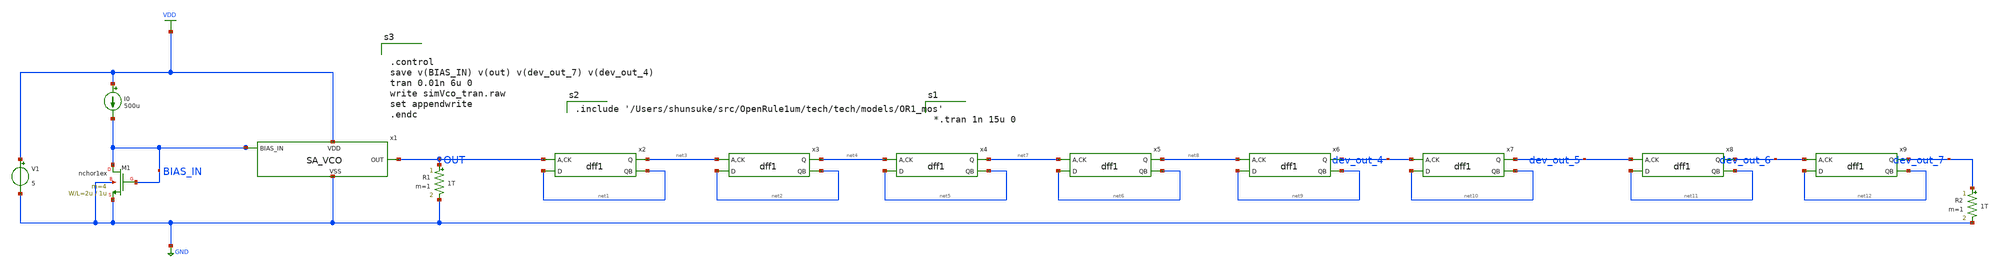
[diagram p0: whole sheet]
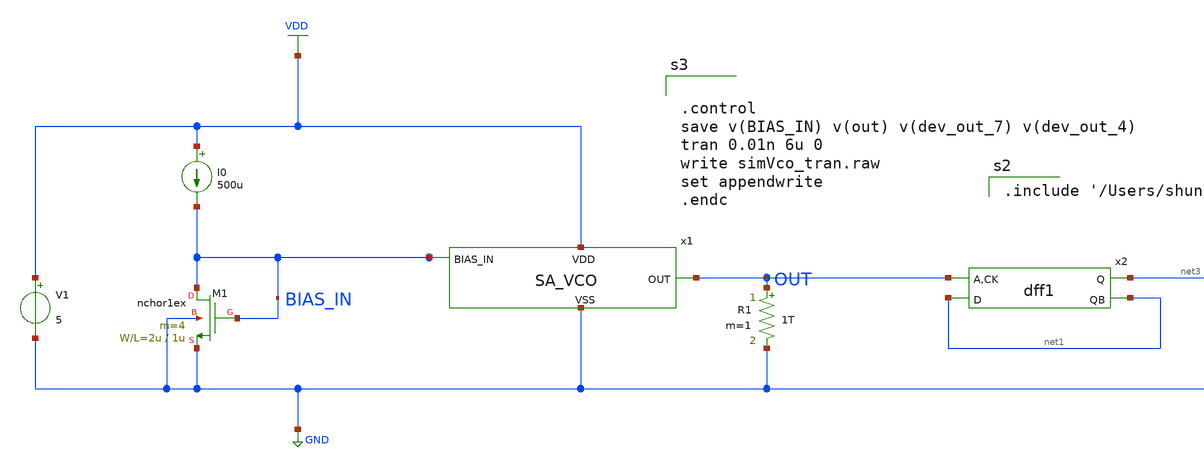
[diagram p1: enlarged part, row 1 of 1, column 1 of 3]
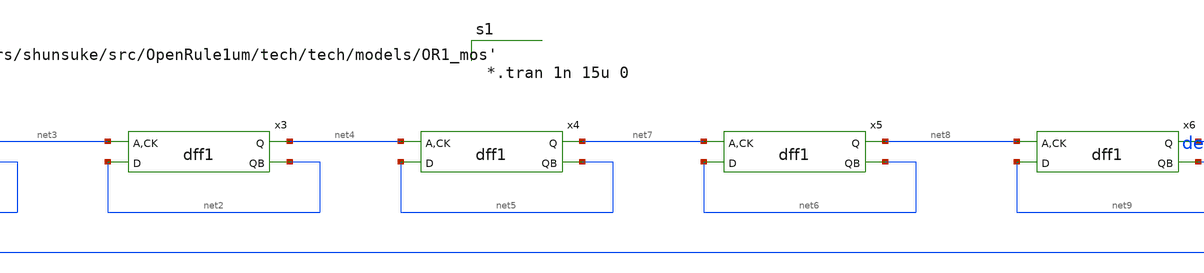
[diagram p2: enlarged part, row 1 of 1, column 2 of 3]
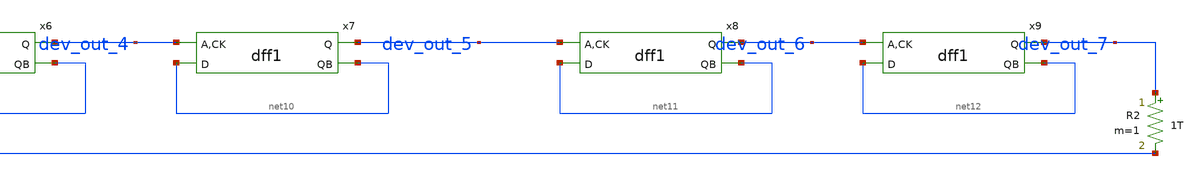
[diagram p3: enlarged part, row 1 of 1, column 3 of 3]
** sch_path: design/.design_bk/xschem/testbench/testVco.sch
**.subckt testVco
V1 VDD GND 5
.save i(v1)
x1 VDD OUT BIAS_IN GND SA_VCO
R1 OUT GND 1T m=1
M1 BIAS_IN BIAS_IN GND GND nchor1ex L=1u W=2u m=4
I0 VDD BIAS_IN 500u
x2 OUT OUT net1 VDD GND net3 net1 dff1
x3 net3 net3 net2 VDD GND net4 net2 dff1
x4 net4 net4 net5 VDD GND net7 net5 dff1
x5 net7 net7 net6 VDD GND net8 net6 dff1
x6 net8 net8 net9 VDD GND dev_out_4 net9 dff1
x7 dev_out_4 dev_out_4 net10 VDD GND dev_out_5 net10 dff1
R2 dev_out_7 GND 1T m=1
x8 dev_out_5 dev_out_5 net11 VDD GND dev_out_6 net11 dff1
x9 dev_out_6 dev_out_6 net12 VDD GND dev_out_7 net12 dff1
**** begin user architecture code


*.tran 1n 15u 0



.include '/Users/shunsuke/src/OpenRule1um/tech/tech/models/OR1_mos'



.control
save v(BIAS_IN) v(out) v(dev_out_7) v(dev_out_4)
tran 0.01n 6u 0
write simVco_tran.raw
set appendwrite
.endc


**** end user architecture code
**.ends

* expanding   symbol:  VCO/SA_VCO.sym # of pins=4
** sym_path: design/xschem/VCO/SA_VCO.sym
** sch_path: design/xschem/VCO/SA_VCO.sch
.subckt SA_VCO VDD OUT BIAS_IN VSS
*.iopin VDD
*.iopin VSS
*.ipin BIAS_IN
*.opin OUT
x1 VDD VDD VSS net1 OUT RO_9
M1 net1 BIAS_IN VSS VSS nchor1ex L=1u W=2u m=4
M2 VSS VSS VSS VSS nchor1ex L=1u W=2u m=2
.ends


* expanding   symbol:  VCO/RO_9.sym # of pins=5
** sym_path: design/.design_bk/xschem/VCO/RO_9.sym
** sch_path: design/.design_bk/xschem/VCO/RO_9.sch
.subckt RO_9 pchSource VDD VSS nchSource OUT
*.iopin pchSource
*.iopin VDD
*.iopin VSS
*.iopin nchSource
*.opin OUT
x2 VDD net1 net2 VSS nchSource SA_VCO_INV
x3 VDD net2 net3 VSS nchSource SA_VCO_INV
x4 VDD net3 net4 VSS nchSource SA_VCO_INV
x5 VDD net4 net5 VSS nchSource SA_VCO_INV
x6 VDD net5 net6 VSS nchSource SA_VCO_INV
x7 VDD net6 net7 VSS nchSource SA_VCO_INV
x8 VDD net7 net8 VSS nchSource SA_VCO_INV
x9 VDD net8 net10 VSS nchSource SA_VCO_INV
x10 VDD net8 OUT VSS VSS SA_VCO_INV
x1 VDD net9 net1 VSS nchSource SA_VCO_INV
x11 VDD net10 net11 VSS nchSource SA_VCO_INV
x12 VDD net11 net12 VSS nchSource SA_VCO_INV
x13 VDD net12 net13 VSS nchSource SA_VCO_INV
x14 VDD net13 net14 VSS nchSource SA_VCO_INV
x15 VDD net14 net15 VSS nchSource SA_VCO_INV
x16 VDD net15 net16 VSS nchSource SA_VCO_INV
x17 VDD net16 net17 VSS nchSource SA_VCO_INV
x18 VDD net17 net9 VSS nchSource SA_VCO_INV
.ends


* expanding   symbol:  VCO/SA_VCO_INV.sym # of pins=5
** sym_path: design/xschem/VCO/SA_VCO_INV.sym
** sch_path: design/xschem/VCO/SA_VCO_INV.sch
.subckt SA_VCO_INV VDD IN OUT VSS nchSource
*.iopin nchSource
*.ipin IN
*.opin OUT
*.iopin VDD
*.iopin VSS
M1 VSS OUT VSS VSS nchor1ex L=3u W=6u m=1
M2 OUT IN VDD VDD pchor1ex L=1u W=4u m=4
M3 OUT IN nchSource VSS nchor1ex L=1u W=4u m=2
.ends

.GLOBAL VDD
.GLOBAL GND
.end
